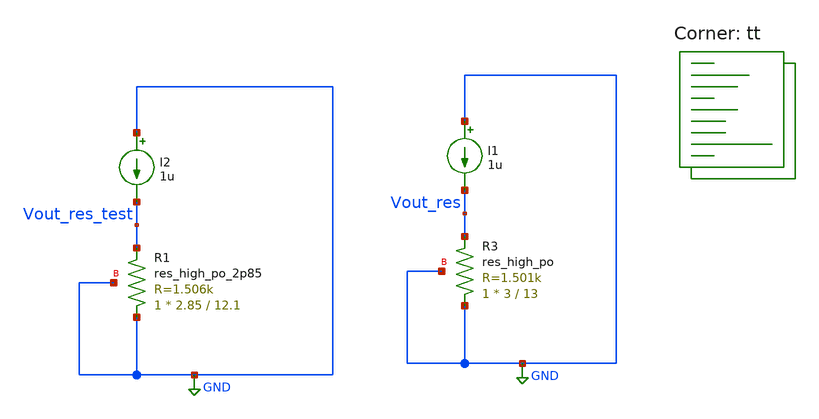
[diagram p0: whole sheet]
** sch_path: design/misc/testing/res.sch
**.subckt res
I1 GND Vout_res 1u
XR3 GND Vout_res GND sky130_fd_pr__res_high_po W=3 L=13 mult=1 m=1
I2 GND Vout_res_test 1u
XR1 GND Vout_res_test GND sky130_fd_pr__res_high_po_2p85 L=12.1 mult=1 m=1
**** begin user architecture code
.lib $::SKYWATER_MODELS/sky130.lib.spice tt


.param temp=27

.dc temp -40 125 1


.save all
.control
run
plot Vout_res Vout_res_test
plot deriv(Vout_res) deriv(Vout_res_test)
.endc



**** end user architecture code
**.ends
.GLOBAL GND
.end
